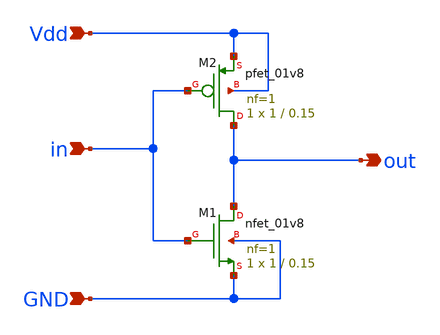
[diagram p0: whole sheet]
** sch_path: RING OSCILLATOR/inverter_gate.sch
**.subckt inverter_gate in out Vdd GND
*.ipin in
*.opin out
*.ipin Vdd
*.ipin GND
XM1 out in GND GND sky130_fd_pr__nfet_01v8 L=0.15 W=1 nf=1 ad='int((nf+1)/2) * W/nf * 0.29' as='int((nf+2)/2) * W/nf * 0.29'
+ pd='2*int((nf+1)/2) * (W/nf + 0.29)' ps='2*int((nf+2)/2) * (W/nf + 0.29)' nrd='0.29 / W' nrs='0.29 / W'
+ sa=0 sb=0 sd=0 mult=1 m=1
XM2 out in Vdd Vdd sky130_fd_pr__pfet_01v8 L=0.15 W=1 nf=1 ad='int((nf+1)/2) * W/nf * 0.29' as='int((nf+2)/2) * W/nf * 0.29'
+ pd='2*int((nf+1)/2) * (W/nf + 0.29)' ps='2*int((nf+2)/2) * (W/nf + 0.29)' nrd='0.29 / W' nrs='0.29 / W'
+ sa=0 sb=0 sd=0 mult=1 m=1
**.ends
.end
